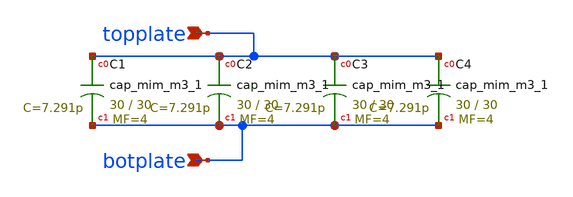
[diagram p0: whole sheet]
** sch_path: design/cap.sch
**.subckt cap botplate topplate
*.ipin botplate
*.ipin topplate
XC1 topplate botplate sky130_fd_pr__cap_mim_m3_1 W=30 L=30 MF=4 m=4
XC2 topplate botplate sky130_fd_pr__cap_mim_m3_1 W=30 L=30 MF=4 m=4
XC3 topplate botplate sky130_fd_pr__cap_mim_m3_1 W=30 L=30 MF=4 m=4
XC4 topplate botplate sky130_fd_pr__cap_mim_m3_1 W=30 L=30 MF=4 m=4
**.ends
.end
